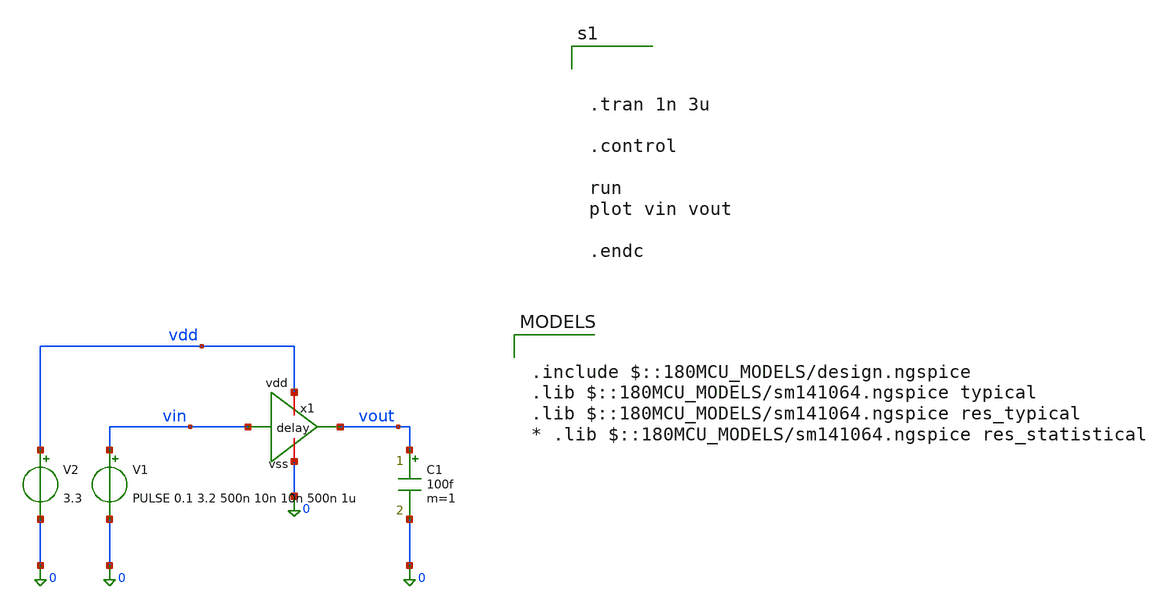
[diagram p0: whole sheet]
** sch_path: General/ADC/delay/delay_tb.sch
**.subckt delay_tb
x1 vdd vin vout 0 delay
C1 vout 0 100f m=1
V1 vin 0 PULSE 0.1 3.2 500n 10n 10n 500n 1u
V2 vdd 0 3.3
**** begin user architecture code

.include $::180MCU_MODELS/design.ngspice
.lib $::180MCU_MODELS/sm141064.ngspice typical
.lib $::180MCU_MODELS/sm141064.ngspice res_typical
* .lib $::180MCU_MODELS/sm141064.ngspice res_statistical




.tran 1n 3u

.control

run
plot vin vout

.endc



**** end user architecture code
**.ends

* expanding   symbol:  ADC/delay/delay.sym # of pins=4
** sym_path: General/ADC/delay/delay.sym
** sch_path: General/ADC/delay/delay.sch
.subckt delay vdd A Y vss
*.ipin A
*.opin Y
*.iopin vdd
*.iopin vss
XM1 net1 A vss vss nfet_03v3 L=5u W=1u nf=1 ad='int((nf+1)/2) * W/nf * 0.18u' as='int((nf+2)/2) * W/nf * 0.18u'
+ pd='2*int((nf+1)/2) * (W/nf + 0.18u)' ps='2*int((nf+2)/2) * (W/nf + 0.18u)' nrd='0.18u / W' nrs='0.18u / W'
+ sa=0 sb=0 sd=0 m=1
XM3 net1 A vdd vdd pfet_03v3 L=5u W=2u nf=1 ad='int((nf+1)/2) * W/nf * 0.18u' as='int((nf+2)/2) * W/nf * 0.18u'
+ pd='2*int((nf+1)/2) * (W/nf + 0.18u)' ps='2*int((nf+2)/2) * (W/nf + 0.18u)' nrd='0.18u / W' nrs='0.18u / W'
+ sa=0 sb=0 sd=0 m=1
XM5 vdd net1 vdd vdd pfet_03v3 L=8u W=8u nf=1 ad='int((nf+1)/2) * W/nf * 0.18u' as='int((nf+2)/2) * W/nf * 0.18u'
+ pd='2*int((nf+1)/2) * (W/nf + 0.18u)' ps='2*int((nf+2)/2) * (W/nf + 0.18u)' nrd='0.18u / W' nrs='0.18u / W'
+ sa=0 sb=0 sd=0 m=1
XM6 vss net1 vss vss nfet_03v3 L=8u W=8u nf=1 ad='int((nf+1)/2) * W/nf * 0.18u' as='int((nf+2)/2) * W/nf * 0.18u'
+ pd='2*int((nf+1)/2) * (W/nf + 0.18u)' ps='2*int((nf+2)/2) * (W/nf + 0.18u)' nrd='0.18u / W' nrs='0.18u / W'
+ sa=0 sb=0 sd=0 m=1
XM7 net3 net2 vss vss nfet_03v3 L=2u W=1u nf=1 ad='int((nf+1)/2) * W/nf * 0.18u' as='int((nf+2)/2) * W/nf * 0.18u'
+ pd='2*int((nf+1)/2) * (W/nf + 0.18u)' ps='2*int((nf+2)/2) * (W/nf + 0.18u)' nrd='0.18u / W' nrs='0.18u / W'
+ sa=0 sb=0 sd=0 m=1
XM8 Y net3 vss vss nfet_03v3 L=0.28u W=5u nf=1 ad='int((nf+1)/2) * W/nf * 0.18u' as='int((nf+2)/2) * W/nf * 0.18u'
+ pd='2*int((nf+1)/2) * (W/nf + 0.18u)' ps='2*int((nf+2)/2) * (W/nf + 0.18u)' nrd='0.18u / W' nrs='0.18u / W'
+ sa=0 sb=0 sd=0 m=1
XM9 net3 net2 vdd vdd pfet_03v3 L=2u W=2u nf=1 ad='int((nf+1)/2) * W/nf * 0.18u' as='int((nf+2)/2) * W/nf * 0.18u'
+ pd='2*int((nf+1)/2) * (W/nf + 0.18u)' ps='2*int((nf+2)/2) * (W/nf + 0.18u)' nrd='0.18u / W' nrs='0.18u / W'
+ sa=0 sb=0 sd=0 m=1
XM10 Y net3 vdd vdd pfet_03v3 L=0.28u W=10u nf=1 ad='int((nf+1)/2) * W/nf * 0.18u' as='int((nf+2)/2) * W/nf * 0.18u'
+ pd='2*int((nf+1)/2) * (W/nf + 0.18u)' ps='2*int((nf+2)/2) * (W/nf + 0.18u)' nrd='0.18u / W' nrs='0.18u / W'
+ sa=0 sb=0 sd=0 m=1
XM11 vdd net2 vdd vdd pfet_03v3 L=8u W=8u nf=1 ad='int((nf+1)/2) * W/nf * 0.18u' as='int((nf+2)/2) * W/nf * 0.18u'
+ pd='2*int((nf+1)/2) * (W/nf + 0.18u)' ps='2*int((nf+2)/2) * (W/nf + 0.18u)' nrd='0.18u / W' nrs='0.18u / W'
+ sa=0 sb=0 sd=0 m=1
XM12 vss net2 vss vss nfet_03v3 L=8u W=8u nf=1 ad='int((nf+1)/2) * W/nf * 0.18u' as='int((nf+2)/2) * W/nf * 0.18u'
+ pd='2*int((nf+1)/2) * (W/nf + 0.18u)' ps='2*int((nf+2)/2) * (W/nf + 0.18u)' nrd='0.18u / W' nrs='0.18u / W'
+ sa=0 sb=0 sd=0 m=1
XM13 vdd net3 vdd vdd pfet_03v3 L=8u W=8u nf=1 ad='int((nf+1)/2) * W/nf * 0.18u' as='int((nf+2)/2) * W/nf * 0.18u'
+ pd='2*int((nf+1)/2) * (W/nf + 0.18u)' ps='2*int((nf+2)/2) * (W/nf + 0.18u)' nrd='0.18u / W' nrs='0.18u / W'
+ sa=0 sb=0 sd=0 m=1
XM14 vss net3 vss vss nfet_03v3 L=8u W=8u nf=1 ad='int((nf+1)/2) * W/nf * 0.18u' as='int((nf+2)/2) * W/nf * 0.18u'
+ pd='2*int((nf+1)/2) * (W/nf + 0.18u)' ps='2*int((nf+2)/2) * (W/nf + 0.18u)' nrd='0.18u / W' nrs='0.18u / W'
+ sa=0 sb=0 sd=0 m=1
XM2 net2 net1 vss vss nfet_03v3 L=5u W=1u nf=1 ad='int((nf+1)/2) * W/nf * 0.18u' as='int((nf+2)/2) * W/nf * 0.18u'
+ pd='2*int((nf+1)/2) * (W/nf + 0.18u)' ps='2*int((nf+2)/2) * (W/nf + 0.18u)' nrd='0.18u / W' nrs='0.18u / W'
+ sa=0 sb=0 sd=0 m=1
XM4 net2 net1 vdd vdd pfet_03v3 L=5u W=2u nf=1 ad='int((nf+1)/2) * W/nf * 0.18u' as='int((nf+2)/2) * W/nf * 0.18u'
+ pd='2*int((nf+1)/2) * (W/nf + 0.18u)' ps='2*int((nf+2)/2) * (W/nf + 0.18u)' nrd='0.18u / W' nrs='0.18u / W'
+ sa=0 sb=0 sd=0 m=1
.ends

.end
